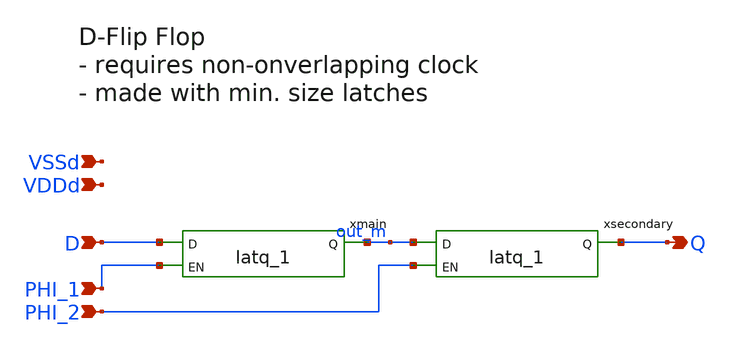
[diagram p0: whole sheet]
** sch_path: designs/klayout/DFF_2phase_1/DFF_2phase_1.sch
**.subckt DFF_2phase_1 D PHI_1 PHI_2 Q VDDd VSSd
*.ipin D
*.ipin PHI_1
*.ipin PHI_2
*.opin Q
*.ipin VDDd
*.ipin VSSd
xmain D PHI_1 out_m VDDd VDDd VSSd VSSd gf180mcu_fd_sc_mcu9t5v0__latq_1
xsecondary out_m PHI_2 Q VDDd VDDd VSSd VSSd gf180mcu_fd_sc_mcu9t5v0__latq_1
**.ends
.end
